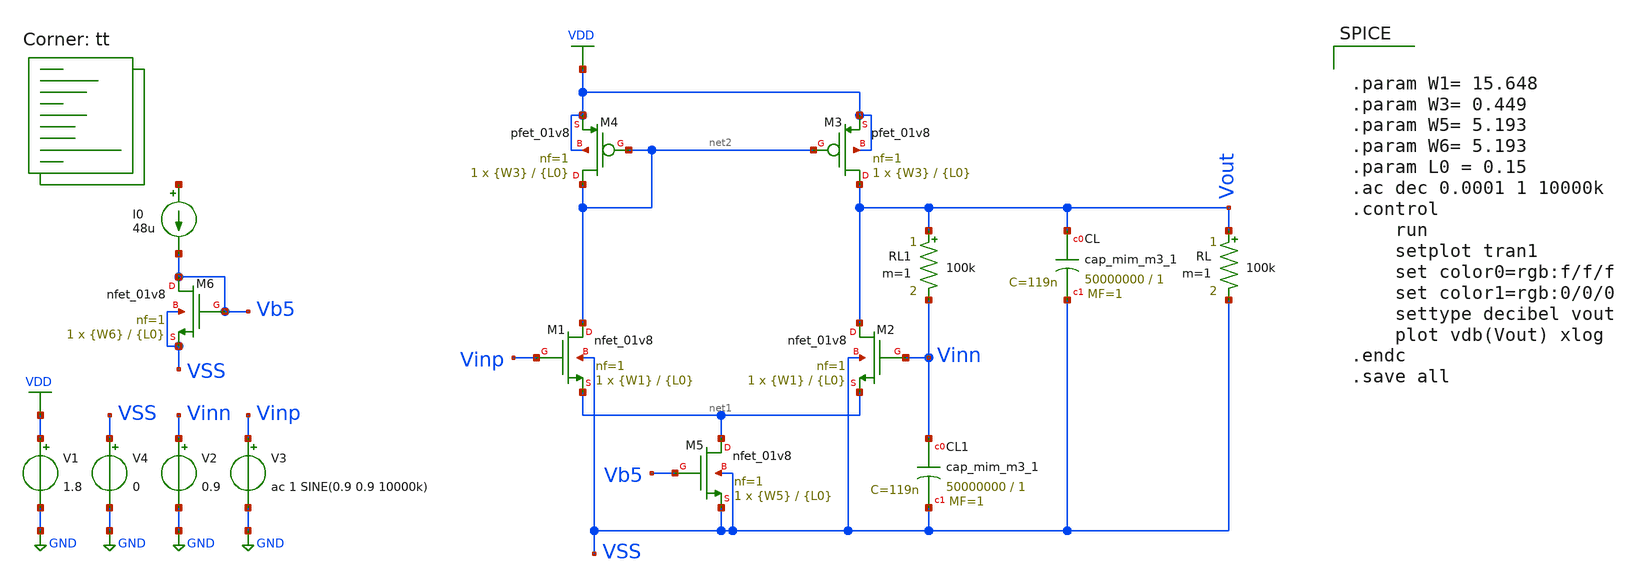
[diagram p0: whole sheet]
** sch_path: opamp_design/simple_one_stage_opamp/simple_one_stage_opamp.sch
**.subckt simple_one_stage_opamp
XM1 net2 Vinp net1 VSS sky130_fd_pr__nfet_01v8 L={L0} W={W1} nf=1 ad='int((nf+1)/2) * W/nf * 0.29' as='int((nf+2)/2) * W/nf * 0.29'
+ pd='2*int((nf+1)/2) * (W/nf + 0.29)' ps='2*int((nf+2)/2) * (W/nf + 0.29)' nrd='0.29 / W' nrs='0.29 / W'
+ sa=0 sb=0 sd=0 mult=1 m=1
XM4 net2 net2 VDD VDD sky130_fd_pr__pfet_01v8 L={L0} W={W3} nf=1 ad='int((nf+1)/2) * W/nf * 0.29' as='int((nf+2)/2) * W/nf * 0.29'
+ pd='2*int((nf+1)/2) * (W/nf + 0.29)' ps='2*int((nf+2)/2) * (W/nf + 0.29)' nrd='0.29 / W' nrs='0.29 / W'
+ sa=0 sb=0 sd=0 mult=1 m=1
XM2 Vout Vinn net1 VSS sky130_fd_pr__nfet_01v8 L={L0} W={W1} nf=1 ad='int((nf+1)/2) * W/nf * 0.29' as='int((nf+2)/2) * W/nf * 0.29'
+ pd='2*int((nf+1)/2) * (W/nf + 0.29)' ps='2*int((nf+2)/2) * (W/nf + 0.29)' nrd='0.29 / W' nrs='0.29 / W'
+ sa=0 sb=0 sd=0 mult=1 m=1
XM3 Vout net2 VDD VDD sky130_fd_pr__pfet_01v8 L={L0} W={W3} nf=1 ad='int((nf+1)/2) * W/nf * 0.29' as='int((nf+2)/2) * W/nf * 0.29'
+ pd='2*int((nf+1)/2) * (W/nf + 0.29)' ps='2*int((nf+2)/2) * (W/nf + 0.29)' nrd='0.29 / W' nrs='0.29 / W'
+ sa=0 sb=0 sd=0 mult=1 m=1
XM5 net1 Vb5 VSS VSS sky130_fd_pr__nfet_01v8 L={L0} W={W5} nf=1 ad='int((nf+1)/2) * W/nf * 0.29' as='int((nf+2)/2) * W/nf * 0.29'
+ pd='2*int((nf+1)/2) * (W/nf + 0.29)' ps='2*int((nf+2)/2) * (W/nf + 0.29)' nrd='0.29 / W' nrs='0.29 / W'
+ sa=0 sb=0 sd=0 mult=1 m=1
V1 VDD GND 1.8
XCL Vout VSS sky130_fd_pr__cap_mim_m3_1 W=50000000 L=1 MF=1 m=1
V2 Vinn GND 0.9
V3 Vinp GND ac 1 SINE(0.9 0.9 10000k)
V4 VSS GND 0
XM6 Vb5 Vb5 VSS VSS sky130_fd_pr__nfet_01v8 L={L0} W={W6} nf=1 ad='int((nf+1)/2) * W/nf * 0.29' as='int((nf+2)/2) * W/nf * 0.29'
+ pd='2*int((nf+1)/2) * (W/nf + 0.29)' ps='2*int((nf+2)/2) * (W/nf + 0.29)' nrd='0.29 / W' nrs='0.29 / W'
+ sa=0 sb=0 sd=0 mult=1 m=1
I0 net3 Vb5 48u
RL Vout VSS 100k m=1
XCL1 Vinn VSS sky130_fd_pr__cap_mim_m3_1 W=50000000 L=1 MF=1 m=1
RL1 Vout Vinn 100k m=1
**** begin user architecture code


.param W1= 15.648
.param W3= 0.449
.param W5= 5.193
.param W6= 5.193
.param L0 = 0.15
.ac dec 0.0001 1 10000k
.control
	run
	setplot tran1
	set color0=rgb:f/f/f
	set color1=rgb:0/0/0
	settype decibel vout
	plot vdb(Vout) xlog
.endc
.save all


.lib $::SKYWATER_MODELS/sky130.lib.spice tt
**** end user architecture code
**.ends
.GLOBAL VDD
.GLOBAL GND
.end
